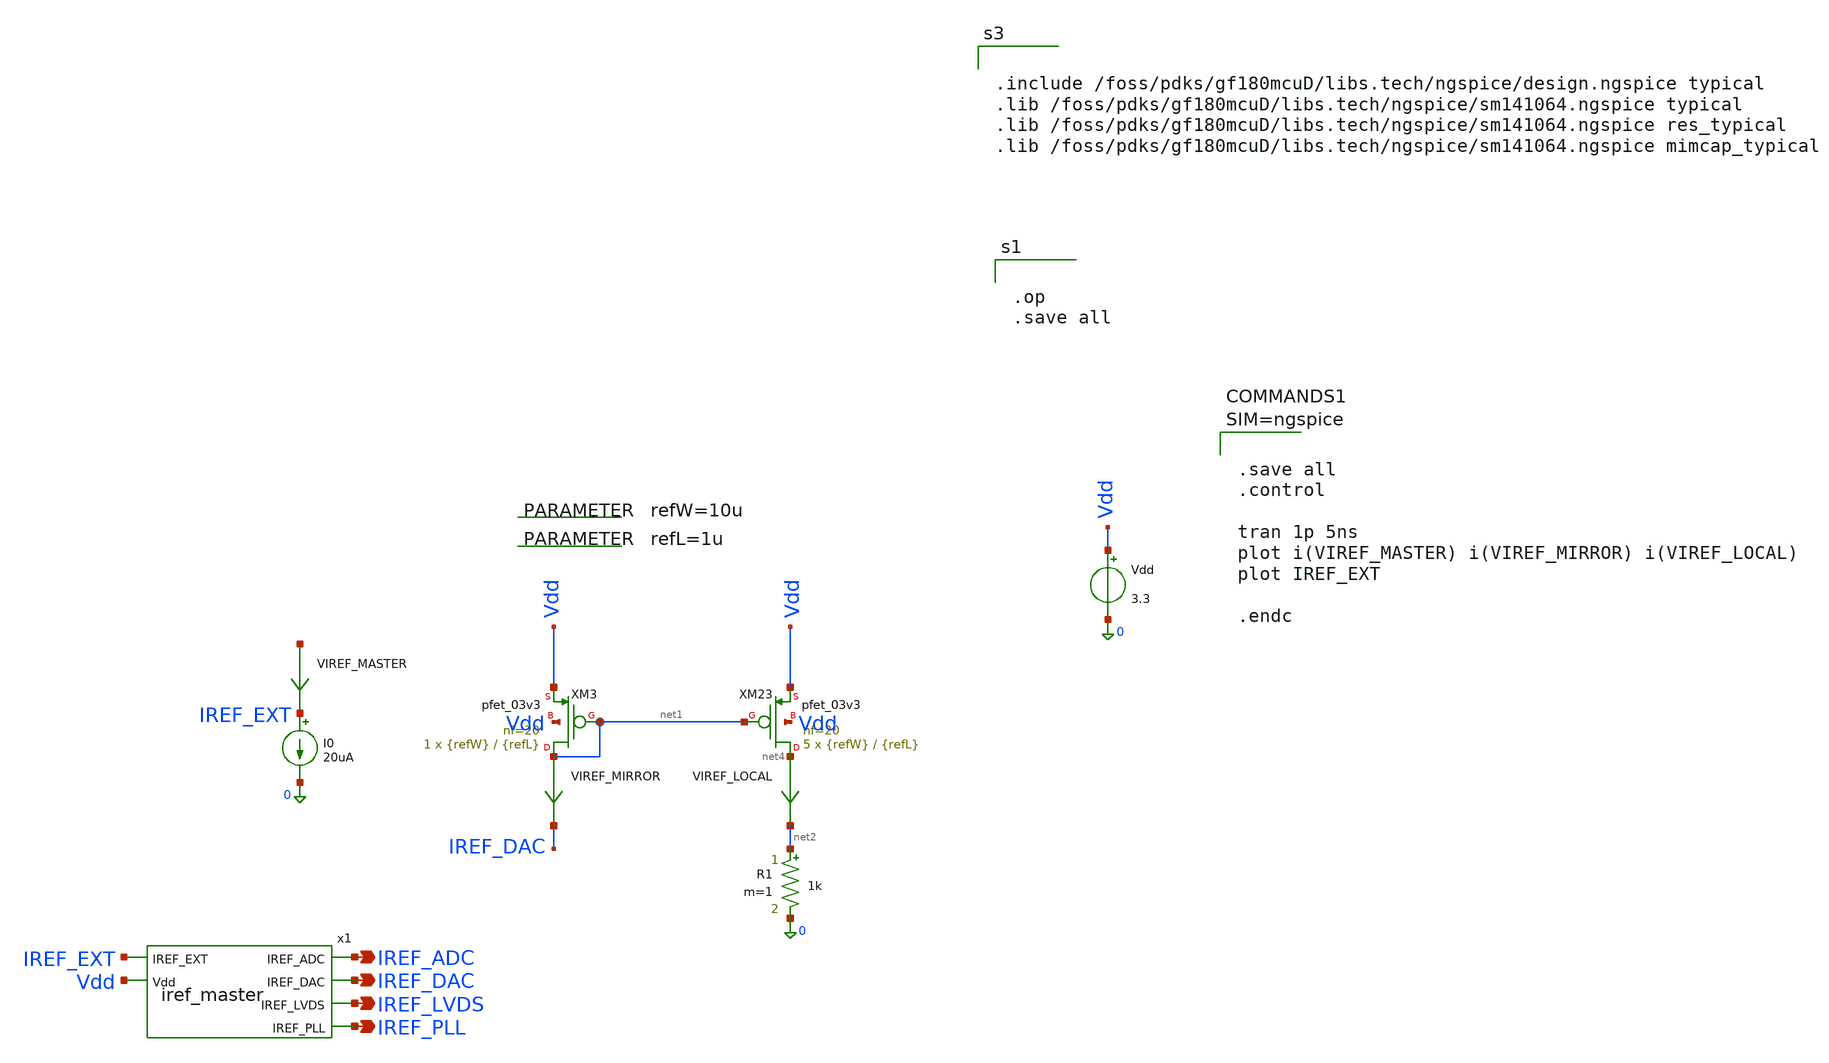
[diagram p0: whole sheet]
** sch_path: blocks/top/test_iref_master.sch
**.subckt test_iref_master IREF_ADC IREF_DAC IREF_LVDS IREF_PLL
*.opin IREF_ADC
*.opin IREF_DAC
*.opin IREF_LVDS
*.opin IREF_PLL
.param refW=10u
.param refL=1u
I0 IREF_EXT 0 20uA
XM3 net1 net1 Vdd Vdd pfet_03v3 L={refL} W={refW} nf=20 ad='int((nf+1)/2) * W/nf * 0.18u' as='int((nf+2)/2) * W/nf * 0.18u'
+ pd='2*int((nf+1)/2) * (W/nf + 0.18u)' ps='2*int((nf+2)/2) * (W/nf + 0.18u)' nrd='0.18u / W' nrs='0.18u / W'
+ sa=0 sb=0 sd=0 m=1
VIREF_MIRROR net1 IREF_DAC 0
.save i(viref_mirror)
Vdd Vdd 0 3.3
.save i(vdd)
VIREF_MASTER net3 IREF_EXT 0
.save i(viref_master)
XM23 net4 net1 Vdd Vdd pfet_03v3 L={refL} W={refW} nf=20 ad='int((nf+1)/2) * W/nf * 0.18u' as='int((nf+2)/2) * W/nf * 0.18u'
+ pd='2*int((nf+1)/2) * (W/nf + 0.18u)' ps='2*int((nf+2)/2) * (W/nf + 0.18u)' nrd='0.18u / W' nrs='0.18u / W'
+ sa=0 sb=0 sd=0 m=5
VIREF_LOCAL net4 net2 0
.save i(viref_local)
x1 IREF_ADC IREF_EXT Vdd IREF_DAC IREF_LVDS IREF_PLL iref_master
R1 net2 0 1k m=1
**** begin user architecture code



.save all
.control

tran 1p 5ns
plot i(VIREF_MASTER) i(VIREF_MIRROR) i(VIREF_LOCAL)
plot IREF_EXT

.endc





.op
.save all




.include /foss/pdks/gf180mcuD/libs.tech/ngspice/design.ngspice typical
.lib /foss/pdks/gf180mcuD/libs.tech/ngspice/sm141064.ngspice typical
.lib /foss/pdks/gf180mcuD/libs.tech/ngspice/sm141064.ngspice res_typical
.lib /foss/pdks/gf180mcuD/libs.tech/ngspice/sm141064.ngspice mimcap_typical


**** end user architecture code
**.ends

* expanding   symbol:  /foss/designs/top/iref_master.sym # of pins=6
** sym_path: blocks/top/iref_master.sym
** sch_path: blocks/top/iref_master.sch
.subckt iref_master IREF_ADC IREF_EXT Vdd IREF_DAC IREF_LVDS IREF_PLL
*.opin IREF_ADC
*.opin IREF_DAC
*.ipin Vdd
*.ipin IREF_EXT
*.opin IREF_LVDS
*.opin IREF_PLL
XM1 VP_CAS VP_CAS Vdd Vdd pfet_03v3 L={refL} W={refW} nf=20 ad='int((nf+1)/2) * W/nf * 0.18u' as='int((nf+2)/2) * W/nf * 0.18u'
+ pd='2*int((nf+1)/2) * (W/nf + 0.18u)' ps='2*int((nf+2)/2) * (W/nf + 0.18u)' nrd='0.18u / W' nrs='0.18u / W'
+ sa=0 sb=0 sd=0 m=1
XM2 net1 net1 VP_CAS Vdd pfet_03v3 L={refL} W={refW} nf=20 ad='int((nf+1)/2) * W/nf * 0.18u' as='int((nf+2)/2) * W/nf * 0.18u'
+ pd='2*int((nf+1)/2) * (W/nf + 0.18u)' ps='2*int((nf+2)/2) * (W/nf + 0.18u)' nrd='0.18u / W' nrs='0.18u / W'
+ sa=0 sb=0 sd=0 m=1
XM3 net2 VP_CAS Vdd Vdd pfet_03v3 L={refL} W={refW} nf=20 ad='int((nf+1)/2) * W/nf * 0.18u' as='int((nf+2)/2) * W/nf * 0.18u'
+ pd='2*int((nf+1)/2) * (W/nf + 0.18u)' ps='2*int((nf+2)/2) * (W/nf + 0.18u)' nrd='0.18u / W' nrs='0.18u / W'
+ sa=0 sb=0 sd=0 m=1
XM21 VN_MIRR net1 net2 Vdd pfet_03v3 L={refL} W={refW} nf=20 ad='int((nf+1)/2) * W/nf * 0.18u' as='int((nf+2)/2) * W/nf * 0.18u'
+ pd='2*int((nf+1)/2) * (W/nf + 0.18u)' ps='2*int((nf+2)/2) * (W/nf + 0.18u)' nrd='0.18u / W' nrs='0.18u / W'
+ sa=0 sb=0 sd=0 m=1
XM22 VN_MIRR VN_MIRR 0 0 nfet_03v3 L={refL*4} W={refW} nf=10 ad='int((nf+1)/2) * W/nf * 0.18u' as='int((nf+2)/2) * W/nf * 0.18u'
+ pd='2*int((nf+1)/2) * (W/nf + 0.18u)' ps='2*int((nf+2)/2) * (W/nf + 0.18u)' nrd='0.18u / W' nrs='0.18u / W'
+ sa=0 sb=0 sd=0 m=1
XM23 net3 VP_CAS Vdd Vdd pfet_03v3 L={refL} W={refW} nf=20 ad='int((nf+1)/2) * W/nf * 0.18u' as='int((nf+2)/2) * W/nf * 0.18u'
+ pd='2*int((nf+1)/2) * (W/nf + 0.18u)' ps='2*int((nf+2)/2) * (W/nf + 0.18u)' nrd='0.18u / W' nrs='0.18u / W'
+ sa=0 sb=0 sd=0 m=1
XM24 VN_CAS net1 net3 Vdd pfet_03v3 L={refL} W={refW} nf=20 ad='int((nf+1)/2) * W/nf * 0.18u' as='int((nf+2)/2) * W/nf * 0.18u'
+ pd='2*int((nf+1)/2) * (W/nf + 0.18u)' ps='2*int((nf+2)/2) * (W/nf + 0.18u)' nrd='0.18u / W' nrs='0.18u / W'
+ sa=0 sb=0 sd=0 m=1
XM25 net4 VN_CAS 0 0 nfet_03v3 L={refL} W={refW} nf=10 ad='int((nf+1)/2) * W/nf * 0.18u' as='int((nf+2)/2) * W/nf * 0.18u'
+ pd='2*int((nf+1)/2) * (W/nf + 0.18u)' ps='2*int((nf+2)/2) * (W/nf + 0.18u)' nrd='0.18u / W' nrs='0.18u / W'
+ sa=0 sb=0 sd=0 m=1
XM26 VN_CAS VN_MIRR net4 0 nfet_03v3 L={refL} W={refW} nf=10 ad='int((nf+1)/2) * W/nf * 0.18u' as='int((nf+2)/2) * W/nf * 0.18u'
+ pd='2*int((nf+1)/2) * (W/nf + 0.18u)' ps='2*int((nf+2)/2) * (W/nf + 0.18u)' nrd='0.18u / W' nrs='0.18u / W'
+ sa=0 sb=0 sd=0 m=1
.param refW=10u
.param refL=1u
VIREF_MASTER net1 IREF_EXT 0
.save i(viref_master)
XM30 net5 VN_CAS 0 0 nfet_03v3 L={refL} W={refW} nf=10 ad='int((nf+1)/2) * W/nf * 0.18u' as='int((nf+2)/2) * W/nf * 0.18u'
+ pd='2*int((nf+1)/2) * (W/nf + 0.18u)' ps='2*int((nf+2)/2) * (W/nf + 0.18u)' nrd='0.18u / W' nrs='0.18u / W'
+ sa=0 sb=0 sd=0 m=1
XM31 IREF_ADC VN_MIRR net5 0 nfet_03v3 L={refL} W={refW} nf=10 ad='int((nf+1)/2) * W/nf * 0.18u' as='int((nf+2)/2) * W/nf * 0.18u'
+ pd='2*int((nf+1)/2) * (W/nf + 0.18u)' ps='2*int((nf+2)/2) * (W/nf + 0.18u)' nrd='0.18u / W' nrs='0.18u / W'
+ sa=0 sb=0 sd=0 m=1
XM32 net6 VN_CAS 0 0 nfet_03v3 L={refL} W={refW} nf=10 ad='int((nf+1)/2) * W/nf * 0.18u' as='int((nf+2)/2) * W/nf * 0.18u'
+ pd='2*int((nf+1)/2) * (W/nf + 0.18u)' ps='2*int((nf+2)/2) * (W/nf + 0.18u)' nrd='0.18u / W' nrs='0.18u / W'
+ sa=0 sb=0 sd=0 m=1
XM33 IREF_DAC VN_MIRR net6 0 nfet_03v3 L={refL} W={refW} nf=10 ad='int((nf+1)/2) * W/nf * 0.18u' as='int((nf+2)/2) * W/nf * 0.18u'
+ pd='2*int((nf+1)/2) * (W/nf + 0.18u)' ps='2*int((nf+2)/2) * (W/nf + 0.18u)' nrd='0.18u / W' nrs='0.18u / W'
+ sa=0 sb=0 sd=0 m=1
XM34 net7 VN_CAS 0 0 nfet_03v3 L={refL} W={refW} nf=10 ad='int((nf+1)/2) * W/nf * 0.18u' as='int((nf+2)/2) * W/nf * 0.18u'
+ pd='2*int((nf+1)/2) * (W/nf + 0.18u)' ps='2*int((nf+2)/2) * (W/nf + 0.18u)' nrd='0.18u / W' nrs='0.18u / W'
+ sa=0 sb=0 sd=0 m=1
XM35 IREF_LVDS VN_MIRR net7 0 nfet_03v3 L={refL} W={refW} nf=10 ad='int((nf+1)/2) * W/nf * 0.18u' as='int((nf+2)/2) * W/nf * 0.18u'
+ pd='2*int((nf+1)/2) * (W/nf + 0.18u)' ps='2*int((nf+2)/2) * (W/nf + 0.18u)' nrd='0.18u / W' nrs='0.18u / W'
+ sa=0 sb=0 sd=0 m=1
XM36 net8 VN_CAS 0 0 nfet_03v3 L={refL} W={refW} nf=10 ad='int((nf+1)/2) * W/nf * 0.18u' as='int((nf+2)/2) * W/nf * 0.18u'
+ pd='2*int((nf+1)/2) * (W/nf + 0.18u)' ps='2*int((nf+2)/2) * (W/nf + 0.18u)' nrd='0.18u / W' nrs='0.18u / W'
+ sa=0 sb=0 sd=0 m=1
XM37 IREF_PLL VN_MIRR net8 0 nfet_03v3 L={refL} W={refW} nf=10 ad='int((nf+1)/2) * W/nf * 0.18u' as='int((nf+2)/2) * W/nf * 0.18u'
+ pd='2*int((nf+1)/2) * (W/nf + 0.18u)' ps='2*int((nf+2)/2) * (W/nf + 0.18u)' nrd='0.18u / W' nrs='0.18u / W'
+ sa=0 sb=0 sd=0 m=1
.ends

.end
